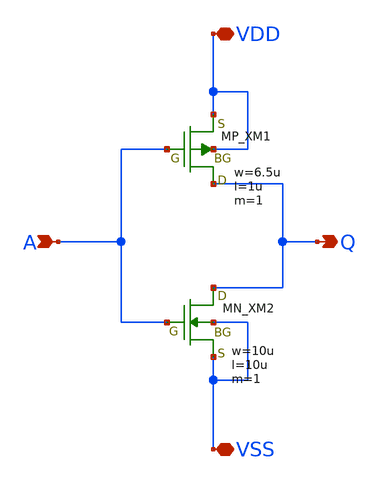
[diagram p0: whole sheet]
** sch_path: schematic/20250924_OSS_Workshop/Qdai/inverter_MUX_01/inv_yano.sch
**.subckt inv_yano VDD VSS Q A
*.iopin VDD
*.iopin VSS
*.opin Q
*.ipin A
XM1 Q A VDD VDD PMOS w=6.5u l=1u as=0 ad=0 ps=0 pd=0 nrd=0 nrs=0 m=1
XM2 Q A VSS VSS NMOS w=10u l=10u as=0 ad=0 ps=0 pd=0 nrd=0 nrs=0 m=1
**.ends
.end
